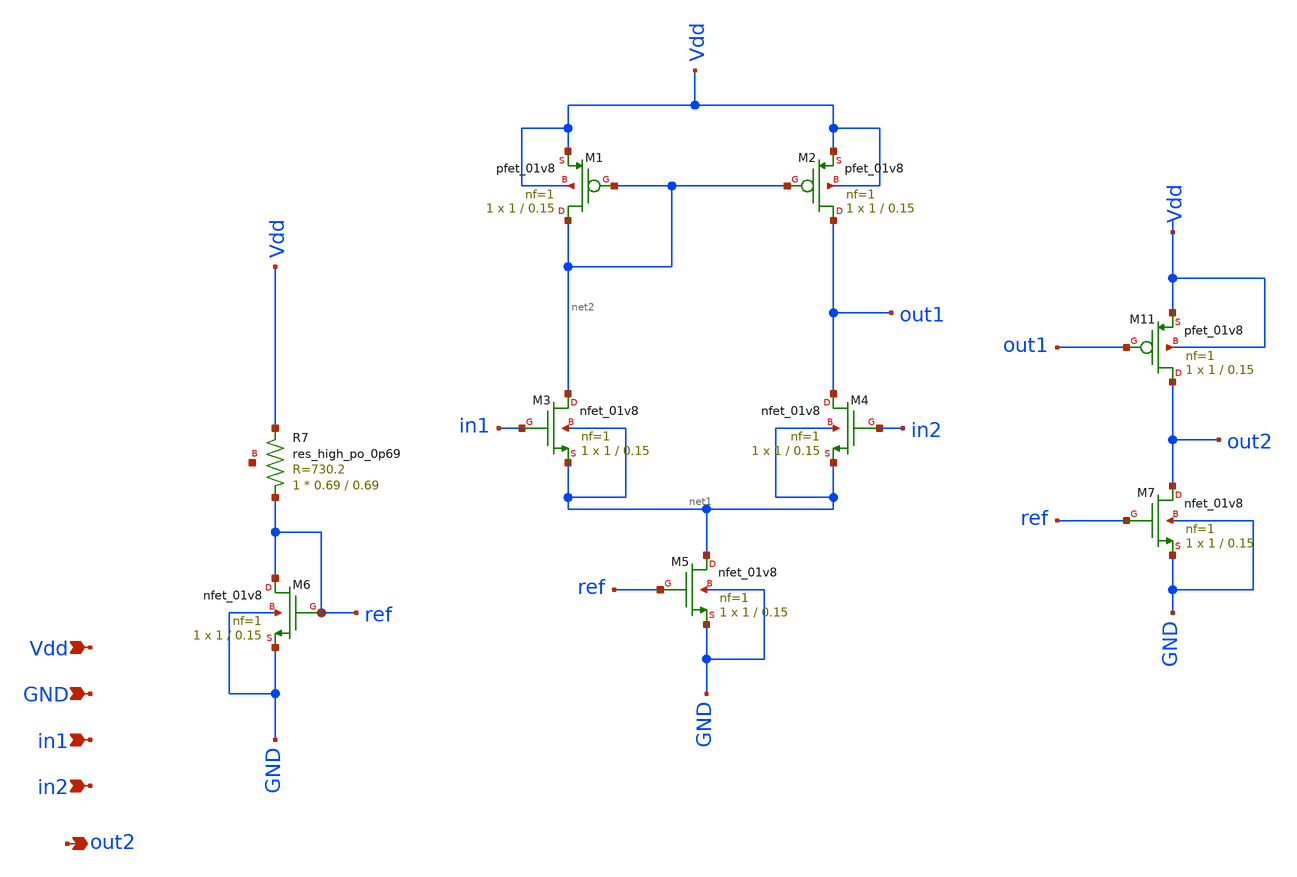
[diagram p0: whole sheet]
** sch_path: VoltageBuff.sch
**.subckt VoltageBuff Vdd GND in1 in2 out2
*.ipin Vdd
*.ipin GND
*.ipin in1
*.ipin in2
*.opin out2
XM3 net2 in1 net1 net1 sky130_fd_pr__nfet_01v8 L=0.15 W=1 nf=1 ad='int((1 + 1)/2) * 1 / 1 * 0.29' as='int((1 + 2)/2) * 1 / 1 * 0.29'
+ pd='2*int((1 + 1)/2) * (1 / 1 + 0.29)' ps='2*int((1 + 2)/2) * (1 / 1 + 0.29)' nrd='0.29 / 1 ' nrs='0.29 / 1 '
+ sa=0 sb=0 sd=0 mult=1 m=1
XM4 out1 in2 net1 net1 sky130_fd_pr__nfet_01v8 L=0.15 W=1 nf=1 ad='int((1 + 1)/2) * 1 / 1 * 0.29' as='int((1 + 2)/2) * 1 / 1 * 0.29'
+ pd='2*int((1 + 1)/2) * (1 / 1 + 0.29)' ps='2*int((1 + 2)/2) * (1 / 1 + 0.29)' nrd='0.29 / 1 ' nrs='0.29 / 1 '
+ sa=0 sb=0 sd=0 mult=1 m=1
XM5 net1 ref GND GND sky130_fd_pr__nfet_01v8 L=0.15 W=1 nf=1 ad='int((1 + 1)/2) * 1 / 1 * 0.29' as='int((1 + 2)/2) * 1 / 1 * 0.29'
+ pd='2*int((1 + 1)/2) * (1 / 1 + 0.29)' ps='2*int((1 + 2)/2) * (1 / 1 + 0.29)' nrd='0.29 / 1 ' nrs='0.29 / 1 '
+ sa=0 sb=0 sd=0 mult=1 m=1
XR7 ref Vdd net3 sky130_fd_pr__res_high_po_0p69 L=0.69 mult=1 m=1
XM6 ref ref GND GND sky130_fd_pr__nfet_01v8 L=0.15 W=1 nf=1 ad='int((1 + 1)/2) * 1 / 1 * 0.29' as='int((1 + 2)/2) * 1 / 1 * 0.29'
+ pd='2*int((1 + 1)/2) * (1 / 1 + 0.29)' ps='2*int((1 + 2)/2) * (1 / 1 + 0.29)' nrd='0.29 / 1 ' nrs='0.29 / 1 '
+ sa=0 sb=0 sd=0 mult=1 m=1
XM11 out2 out1 Vdd Vdd sky130_fd_pr__pfet_01v8 L=0.15 W=1 nf=1 ad='int((nf+1)/2) * W/nf * 0.29' as='int((nf+2)/2) * W/nf * 0.29'
+ pd='2*int((nf+1)/2) * (W/nf + 0.29)' ps='2*int((nf+2)/2) * (W/nf + 0.29)' nrd='0.29 / W' nrs='0.29 / W'
+ sa=0 sb=0 sd=0 mult=1 m=1
XM1 net2 net2 Vdd Vdd sky130_fd_pr__pfet_01v8 L=0.15 W=1 nf=1 ad='int((nf+1)/2) * W/nf * 0.29' as='int((nf+2)/2) * W/nf * 0.29'
+ pd='2*int((nf+1)/2) * (W/nf + 0.29)' ps='2*int((nf+2)/2) * (W/nf + 0.29)' nrd='0.29 / W' nrs='0.29 / W'
+ sa=0 sb=0 sd=0 mult=1 m=1
XM2 out1 net2 Vdd Vdd sky130_fd_pr__pfet_01v8 L=0.15 W=1 nf=1 ad='int((nf+1)/2) * W/nf * 0.29' as='int((nf+2)/2) * W/nf * 0.29'
+ pd='2*int((nf+1)/2) * (W/nf + 0.29)' ps='2*int((nf+2)/2) * (W/nf + 0.29)' nrd='0.29 / W' nrs='0.29 / W'
+ sa=0 sb=0 sd=0 mult=1 m=1
XM7 out2 ref GND GND sky130_fd_pr__nfet_01v8 L=0.15 W=1 nf=1 ad='int((1 + 1)/2) * 1 / 1 * 0.29' as='int((1 + 2)/2) * 1 / 1 * 0.29'
+ pd='2*int((1 + 1)/2) * (1 / 1 + 0.29)' ps='2*int((1 + 2)/2) * (1 / 1 + 0.29)' nrd='0.29 / 1 ' nrs='0.29 / 1 '
+ sa=0 sb=0 sd=0 mult=1 m=1
**.ends
.end
